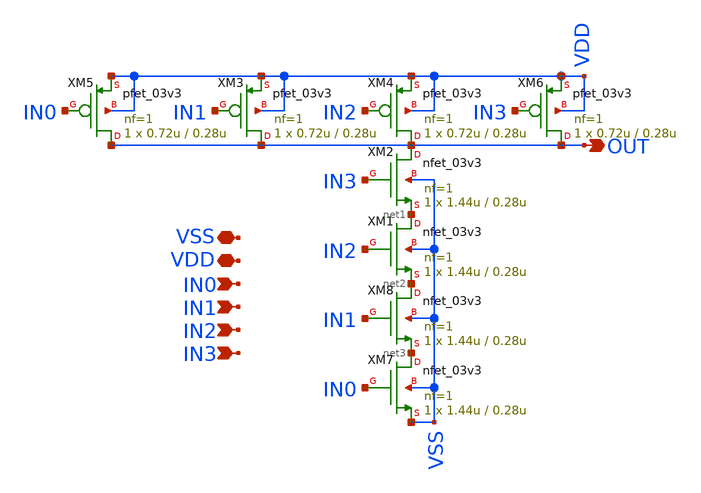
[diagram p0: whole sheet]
** sch_path: CAD4/nand4.sch
**.subckt nand4 VSS VDD IN0 IN1 OUT IN2 IN3
*.iopin VSS
*.iopin VDD
*.ipin IN0
*.ipin IN1
*.opin OUT
*.ipin IN2
*.ipin IN3
XM1 net1 IN2 net2 VSS nfet_03v3 L=0.28u W=1.44u nf=1 ad='int((nf+1)/2) * W/nf * 0.18u' as='int((nf+2)/2) * W/nf * 0.18u'
+ pd='2*int((nf+1)/2) * (W/nf + 0.18u)' ps='2*int((nf+2)/2) * (W/nf + 0.18u)' nrd='0.18u / W' nrs='0.18u / W'
+ sa=0 sb=0 sd=0 m=1
XM2 OUT IN3 net1 VSS nfet_03v3 L=0.28u W=1.44u nf=1 ad='int((nf+1)/2) * W/nf * 0.18u' as='int((nf+2)/2) * W/nf * 0.18u'
+ pd='2*int((nf+1)/2) * (W/nf + 0.18u)' ps='2*int((nf+2)/2) * (W/nf + 0.18u)' nrd='0.18u / W' nrs='0.18u / W'
+ sa=0 sb=0 sd=0 m=1
XM3 OUT IN1 VDD VDD pfet_03v3 L=0.28u W=0.72u nf=1 ad='int((nf+1)/2) * W/nf * 0.18u' as='int((nf+2)/2) * W/nf * 0.18u'
+ pd='2*int((nf+1)/2) * (W/nf + 0.18u)' ps='2*int((nf+2)/2) * (W/nf + 0.18u)' nrd='0.18u / W' nrs='0.18u / W'
+ sa=0 sb=0 sd=0 m=1
XM4 OUT IN2 VDD VDD pfet_03v3 L=0.28u W=0.72u nf=1 ad='int((nf+1)/2) * W/nf * 0.18u' as='int((nf+2)/2) * W/nf * 0.18u'
+ pd='2*int((nf+1)/2) * (W/nf + 0.18u)' ps='2*int((nf+2)/2) * (W/nf + 0.18u)' nrd='0.18u / W' nrs='0.18u / W'
+ sa=0 sb=0 sd=0 m=1
XM5 OUT IN0 VDD VDD pfet_03v3 L=0.28u W=0.72u nf=1 ad='int((nf+1)/2) * W/nf * 0.18u' as='int((nf+2)/2) * W/nf * 0.18u'
+ pd='2*int((nf+1)/2) * (W/nf + 0.18u)' ps='2*int((nf+2)/2) * (W/nf + 0.18u)' nrd='0.18u / W' nrs='0.18u / W'
+ sa=0 sb=0 sd=0 m=1
XM6 OUT IN3 VDD VDD pfet_03v3 L=0.28u W=0.72u nf=1 ad='int((nf+1)/2) * W/nf * 0.18u' as='int((nf+2)/2) * W/nf * 0.18u'
+ pd='2*int((nf+1)/2) * (W/nf + 0.18u)' ps='2*int((nf+2)/2) * (W/nf + 0.18u)' nrd='0.18u / W' nrs='0.18u / W'
+ sa=0 sb=0 sd=0 m=1
XM7 net3 IN0 VSS VSS nfet_03v3 L=0.28u W=1.44u nf=1 ad='int((nf+1)/2) * W/nf * 0.18u' as='int((nf+2)/2) * W/nf * 0.18u'
+ pd='2*int((nf+1)/2) * (W/nf + 0.18u)' ps='2*int((nf+2)/2) * (W/nf + 0.18u)' nrd='0.18u / W' nrs='0.18u / W'
+ sa=0 sb=0 sd=0 m=1
XM8 net2 IN1 net3 VSS nfet_03v3 L=0.28u W=1.44u nf=1 ad='int((nf+1)/2) * W/nf * 0.18u' as='int((nf+2)/2) * W/nf * 0.18u'
+ pd='2*int((nf+1)/2) * (W/nf + 0.18u)' ps='2*int((nf+2)/2) * (W/nf + 0.18u)' nrd='0.18u / W' nrs='0.18u / W'
+ sa=0 sb=0 sd=0 m=1
**.ends
.end
